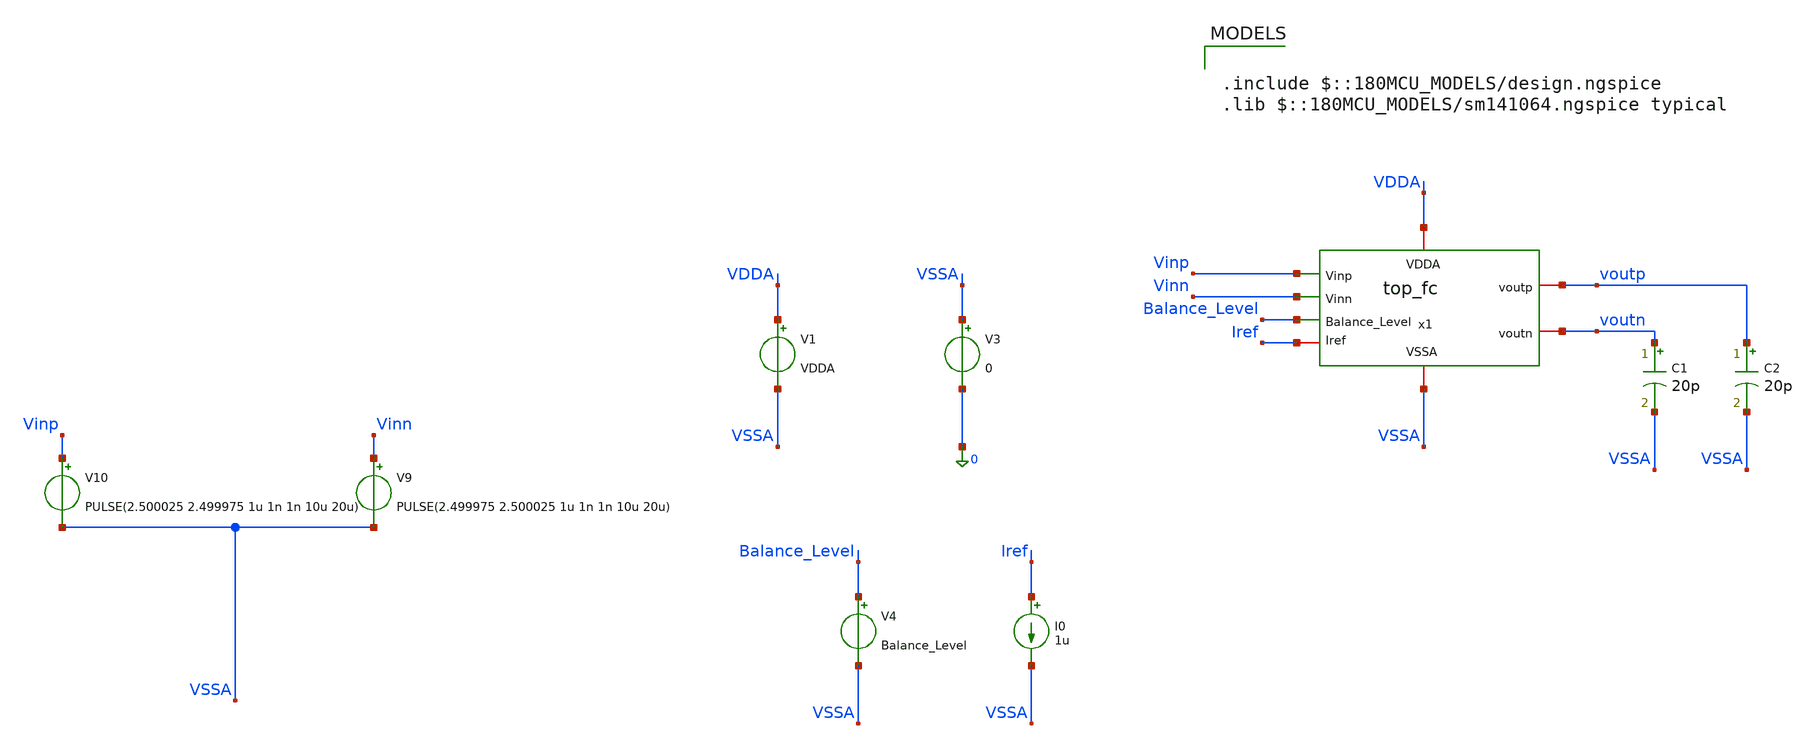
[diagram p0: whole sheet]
** sch_path: Folded_cascode/testbenches/top_fc_tran_tb.sch
**.subckt top_fc_tran_tb
x1 Balance_Level Vinp voutp VDDA voutn Vinn Iref VSSA top_fc
C1 voutn VSSA 20p m=1
C2 voutp VSSA 20p m=1
V1 VDDA VSSA VDDA
V3 VSSA 0 0
V4 Balance_Level VSSA Balance_Level
I0 Iref VSSA 1u
V9 Vinn VSSA PULSE(2.499975 2.500025 1u 1n 1n 10u 20u)
V10 Vinp VSSA PULSE(2.500025 2.499975 1u 1n 1n 10u 20u)
**** begin user architecture code

.include $::180MCU_MODELS/design.ngspice
.lib $::180MCU_MODELS/sm141064.ngspice typical



.temp 27
.param VDDA = 5
.param Balance_Level = 1.5
.param VD = 0

.control
option sparse
set filetype=ascii
set wr_singlescale
set wr_vecnames
save all
save @m.x1.x1.xm1.m0[id]
save @m.x1.x1.xm1.m0[gm]
save @m.x1.x1.xm1.m0[vgs]
save @m.x1.x1.xm1.m0[vds]
save @m.x1.x1.xm1.m0[vth]
save @m.x1.x1.xm1.m0[gds]
save @m.x1.x1.xm1.m0[vdsat]

save @m.x1.x1.xm2.m0[id]
save @m.x1.x1.xm2.m0[gm]
save @m.x1.x1.xm2.m0[vgs]
save @m.x1.x1.xm2.m0[vds]
save @m.x1.x1.xm2.m0[vth]
save @m.x1.x1.xm2.m0[gds]
save @m.x1.x1.xm2.m0[vdsat]

save @m.x1.x1.xm9.m0[id]
save @m.x1.x1.xm9.m0[gm]
save @m.x1.x1.xm9.m0[vgs]
save @m.x1.x1.xm9.m0[vds]
save @m.x1.x1.xm9.m0[vth]
save @m.x1.x1.xm9.m0[gds]
save @m.x1.x1.xm9.m0[vdsat]

save @m.x1.x1.xm8.m0[id]
save @m.x1.x1.xm8.m0[gm]
save @m.x1.x1.xm8.m0[vgs]
save @m.x1.x1.xm8.m0[vds]
save @m.x1.x1.xm8.m0[vth]
save @m.x1.x1.xm8.m0[gds]
save @m.x1.x1.xm8.m0[vdsat]

save @m.x1.x1.xm6.m0[id]
save @m.x1.x1.xm6.m0[gm]
save @m.x1.x1.xm6.m0[vgs]
save @m.x1.x1.xm6.m0[vds]
save @m.x1.x1.xm6.m0[vth]
save @m.x1.x1.xm6.m0[gds]
save @m.x1.x1.xm6.m0[vdsat]

save @m.x1.x1.xm5.m0[id]
save @m.x1.x1.xm5.m0[gm]
save @m.x1.x1.xm5.m0[vgs]
save @m.x1.x1.xm5.m0[vds]
save @m.x1.x1.xm5.m0[vth]
save @m.x1.x1.xm5.m0[gds]
save @m.x1.x1.xm5.m0[vdsat]

save @m.x1.x2.xm1.m0[id]
save @m.x1.x2.xm1.m0[gm]
save @m.x1.x2.xm1.m0[vgs]
save @m.x1.x2.xm1.m0[vds]
save @m.x1.x2.xm1.m0[vth]
save @m.x1.x2.xm1.m0[gds]

save @m.x1.x2.xm2.m0[id]
save @m.x1.x2.xm2.m0[gm]
save @m.x1.x2.xm2.m0[vgs]
save @m.x1.x2.xm2.m0[vds]
save @m.x1.x2.xm2.m0[vth]
save @m.x1.x2.xm2.m0[gds]

save @m.x1.x2.xm3.m0[id]
save @m.x1.x2.xm3.m0[gm]
save @m.x1.x2.xm3.m0[vgs]
save @m.x1.x2.xm3.m0[vds]
save @m.x1.x2.xm3.m0[vth]
save @m.x1.x2.xm3.m0[gds]

save @m.x1.x2.xm4.m0[id]
save @m.x1.x2.xm4.m0[gm]
save @m.x1.x2.xm4.m0[vgs]
save @m.x1.x2.xm4.m0[vds]
save @m.x1.x2.xm4.m0[vth]
save @m.x1.x2.xm4.m0[gds]

save @m.x1.x2.xm5.m0[id]
save @m.x1.x2.xm5.m0[gm]
save @m.x1.x2.xm5.m0[vgs]
save @m.x1.x2.xm5.m0[vds]
save @m.x1.x2.xm5.m0[vth]
save @m.x1.x2.xm5.m0[gds]

save @m.x1.x2.xm6.m0[id]
save @m.x1.x2.xm6.m0[gm]
save @m.x1.x2.xm6.m0[vgs]
save @m.x1.x2.xm6.m0[vds]
save @m.x1.x2.xm6.m0[vth]
save @m.x1.x2.xm6.m0[gds]

save @m.x1.x2.xm7.m0[id]
save @m.x1.x2.xm7.m0[gm]
save @m.x1.x2.xm7.m0[vgs]
save @m.x1.x2.xm7.m0[vds]
save @m.x1.x2.xm7.m0[vth]
save @m.x1.x2.xm7.m0[gds]

save @m.x1.x2.xm8.m0[id]
save @m.x1.x2.xm8.m0[gm]
save @m.x1.x2.xm8.m0[vgs]
save @m.x1.x2.xm8.m0[vds]
save @m.x1.x2.xm8.m0[vth]
save @m.x1.x2.xm8.m0[gds]

save @m.x1.x2.xm9.m0[id]
save @m.x1.x2.xm9.m0[gm]
save @m.x1.x2.xm9.m0[vgs]
save @m.x1.x2.xm9.m0[vds]
save @m.x1.x2.xm9.m0[vth]
save @m.x1.x2.xm9.m0[gds]

save @m.x1.x3.xm1.m0[id]
save @m.x1.x3.xm1.m0[gm]
save @m.x1.x3.xm1.m0[vgs]
save @m.x1.x3.xm1.m0[vds]
save @m.x1.x3.xm1.m0[vth]
save @m.x1.x3.xm1.m0[gds]

save @m.x1.x3.xm2.m0[id]
save @m.x1.x3.xm2.m0[gm]
save @m.x1.x3.xm2.m0[vgs]
save @m.x1.x3.xm2.m0[vds]
save @m.x1.x3.xm2.m0[vth]
save @m.x1.x3.xm2.m0[gds]

save @m.x1.x3.xm3.m0[id]
save @m.x1.x3.xm3.m0[gm]
save @m.x1.x3.xm3.m0[vgs]
save @m.x1.x3.xm3.m0[vds]
save @m.x1.x3.xm3.m0[vth]
save @m.x1.x3.xm3.m0[gds]

save @m.x1.x3.xm4.m0[id]
save @m.x1.x3.xm4.m0[gm]
save @m.x1.x3.xm4.m0[vgs]
save @m.x1.x3.xm4.m0[vds]
save @m.x1.x3.xm4.m0[vth]
save @m.x1.x3.xm4.m0[gds]

save @m.x1.x3.xm5.m0[id]
save @m.x1.x3.xm5.m0[gm]
save @m.x1.x3.xm5.m0[vgs]
save @m.x1.x3.xm5.m0[vds]
save @m.x1.x3.xm5.m0[vth]
save @m.x1.x3.xm5.m0[gds]

save @m.x1.x3.xm6.m0[id]
save @m.x1.x3.xm6.m0[gm]
save @m.x1.x3.xm6.m0[vgs]
save @m.x1.x3.xm6.m0[vds]
save @m.x1.x3.xm6.m0[vth]
save @m.x1.x3.xm6.m0[gds]

save @m.x1.x3.xm7.m0[id]
save @m.x1.x3.xm7.m0[gm]
save @m.x1.x3.xm7.m0[vgs]
save @m.x1.x3.xm7.m0[vds]
save @m.x1.x3.xm7.m0[vth]
save @m.x1.x3.xm7.m0[gds]

save @m.x1.x3.xm8.m0[id]
save @m.x1.x3.xm8.m0[gm]
save @m.x1.x3.xm8.m0[vgs]
save @m.x1.x3.xm8.m0[vds]
save @m.x1.x3.xm8.m0[vth]
save @m.x1.x3.xm8.m0[gds]

save @m.x1.x3.xm9.m0[id]
save @m.x1.x3.xm9.m0[gm]
save @m.x1.x3.xm9.m0[vgs]
save @m.x1.x3.xm9.m0[vds]
save @m.x1.x3.xm9.m0[vth]
save @m.x1.x3.xm9.m0[gds]

save @m.x1.x3.xm10.m0[id]
save @m.x1.x3.xm10.m0[gm]
save @m.x1.x3.xm10.m0[vgs]
save @m.x1.x3.xm10.m0[vds]
save @m.x1.x3.xm10.m0[vth]
save @m.x1.x3.xm10.m0[gds]

save @m.x1.x3.xm11.m0[id]
save @m.x1.x3.xm11.m0[gm]
save @m.x1.x3.xm11.m0[vgs]
save @m.x1.x3.xm11.m0[vds]
save @m.x1.x3.xm11.m0[vth]
save @m.x1.x3.xm11.m0[gds]

save @m.x1.x3.xm12.m0[id]
save @m.x1.x3.xm12.m0[gm]
save @m.x1.x3.xm12.m0[vgs]
save @m.x1.x3.xm12.m0[vds]
save @m.x1.x3.xm12.m0[vth]
save @m.x1.x3.xm12.m0[gds]

save @m.x1.x3.xm13.m0[id]
save @m.x1.x3.xm13.m0[gm]
save @m.x1.x3.xm13.m0[vgs]
save @m.x1.x3.xm13.m0[vds]
save @m.x1.x3.xm13.m0[vth]
save @m.x1.x3.xm13.m0[gds]

save @m.x1.x3.xm14.m0[id]
save @m.x1.x3.xm14.m0[gm]
save @m.x1.x3.xm14.m0[vgs]
save @m.x1.x3.xm14.m0[vds]
save @m.x1.x3.xm14.m0[vth]
save @m.x1.x3.xm14.m0[gds]

save @m.x1.x3.xm15.m0[id]
save @m.x1.x3.xm15.m0[gm]
save @m.x1.x3.xm15.m0[vgs]
save @m.x1.x3.xm15.m0[vds]
save @m.x1.x3.xm15.m0[vth]
save @m.x1.x3.xm15.m0[gds]

save @m.x1.x3.xm16.m0[id]
save @m.x1.x3.xm16.m0[gm]
save @m.x1.x3.xm16.m0[vgs]
save @m.x1.x3.xm16.m0[vds]
save @m.x1.x3.xm16.m0[vth]
save @m.x1.x3.xm16.m0[gds]

save @m.x1.x3.xm17.m0[id]
save @m.x1.x3.xm17.m0[gm]
save @m.x1.x3.xm17.m0[vgs]
save @m.x1.x3.xm17.m0[vds]
save @m.x1.x3.xm17.m0[vth]
save @m.x1.x3.xm17.m0[gds]

save @m.x1.x3.xm18.m0[id]
save @m.x1.x3.xm18.m0[gm]
save @m.x1.x3.xm18.m0[vgs]
save @m.x1.x3.xm18.m0[vds]
save @m.x1.x3.xm18.m0[vth]
save @m.x1.x3.xm18.m0[gds]

save @m.x1.x3.xm21.m0[id]
save @m.x1.x3.xm21.m0[gm]
save @m.x1.x3.xm21.m0[vgs]
save @m.x1.x3.xm21.m0[vds]
save @m.x1.x3.xm21.m0[vth]
save @m.x1.x3.xm21.m0[gds]

save @m.x1.x3.xm22.m0[id]
save @m.x1.x3.xm22.m0[gm]
save @m.x1.x3.xm22.m0[vgs]
save @m.x1.x3.xm22.m0[vds]
save @m.x1.x3.xm22.m0[vth]
save @m.x1.x3.xm22.m0[gds]

op
write top_fc_op_tb.raw all

tran 10n 50u


let vid  = v(vinp)-v(vinn)
let vod  = v(voutp)-v(voutn)
let vocm = (v(voutp)+v(voutn))/2

plot vid
plot vod
plot vocm
plot v(x1.vb4)


write top_fc_tran_tb.raw

.endc


**** end user architecture code
**.ends
.end
